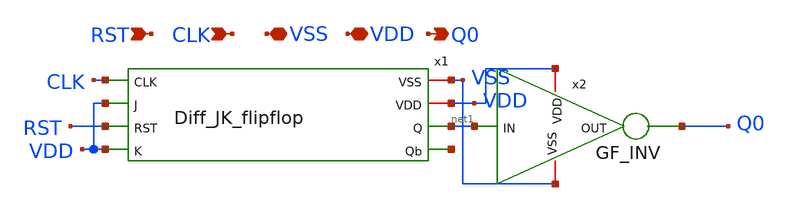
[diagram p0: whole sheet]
** sch_path: Clock_Generator_PAKISTAN_02/Schematics/Diff_Clk_div_2.sch
**.subckt Diff_Clk_div_2 CLK VSS VDD Q0 RST
*.ipin CLK
*.iopin VSS
*.iopin VDD
*.opin Q0
*.ipin RST
x1 CLK VSS VDD net1 VDD net2 RST VDD Diff_JK_flipflop
x2 VSS VDD Q0 net1 GF_INV
**.ends
.end
